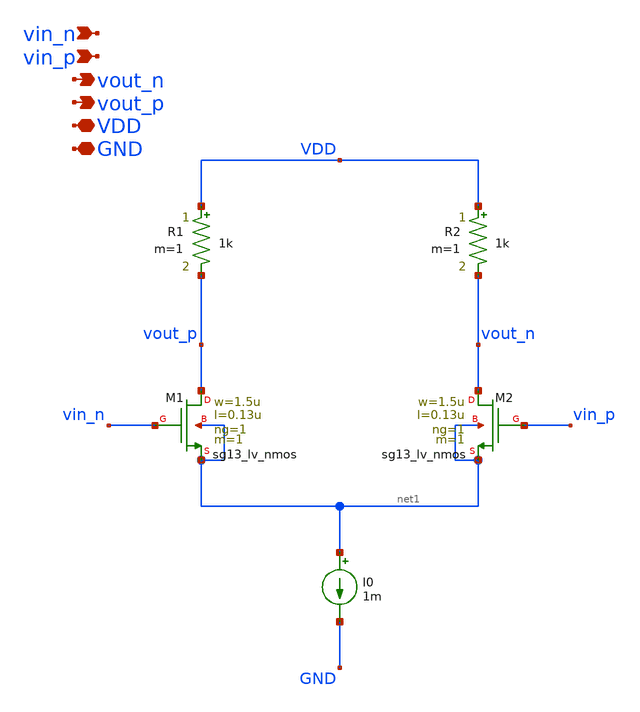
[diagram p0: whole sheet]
** sch_path: 20260718_ring_oscillator/diff_inv.sch
**.subckt diff_inv vout_p VDD GND vout_n vin_p vin_n
*.opin vout_p
*.iopin VDD
*.iopin GND
*.opin vout_n
*.ipin vin_p
*.ipin vin_n
XM1 vout_p vin_n net1 net1 sg13_lv_nmos w=1.5u l=0.13u ng=1 m=1 mm_ok=1
XM2 vout_n vin_p net1 net1 sg13_lv_nmos w=1.5u l=0.13u ng=1 m=1 mm_ok=1
R1 VDD vout_p 1k m=1
R2 VDD vout_n 1k m=1
I0 net1 GND 1m
**.ends
.end
